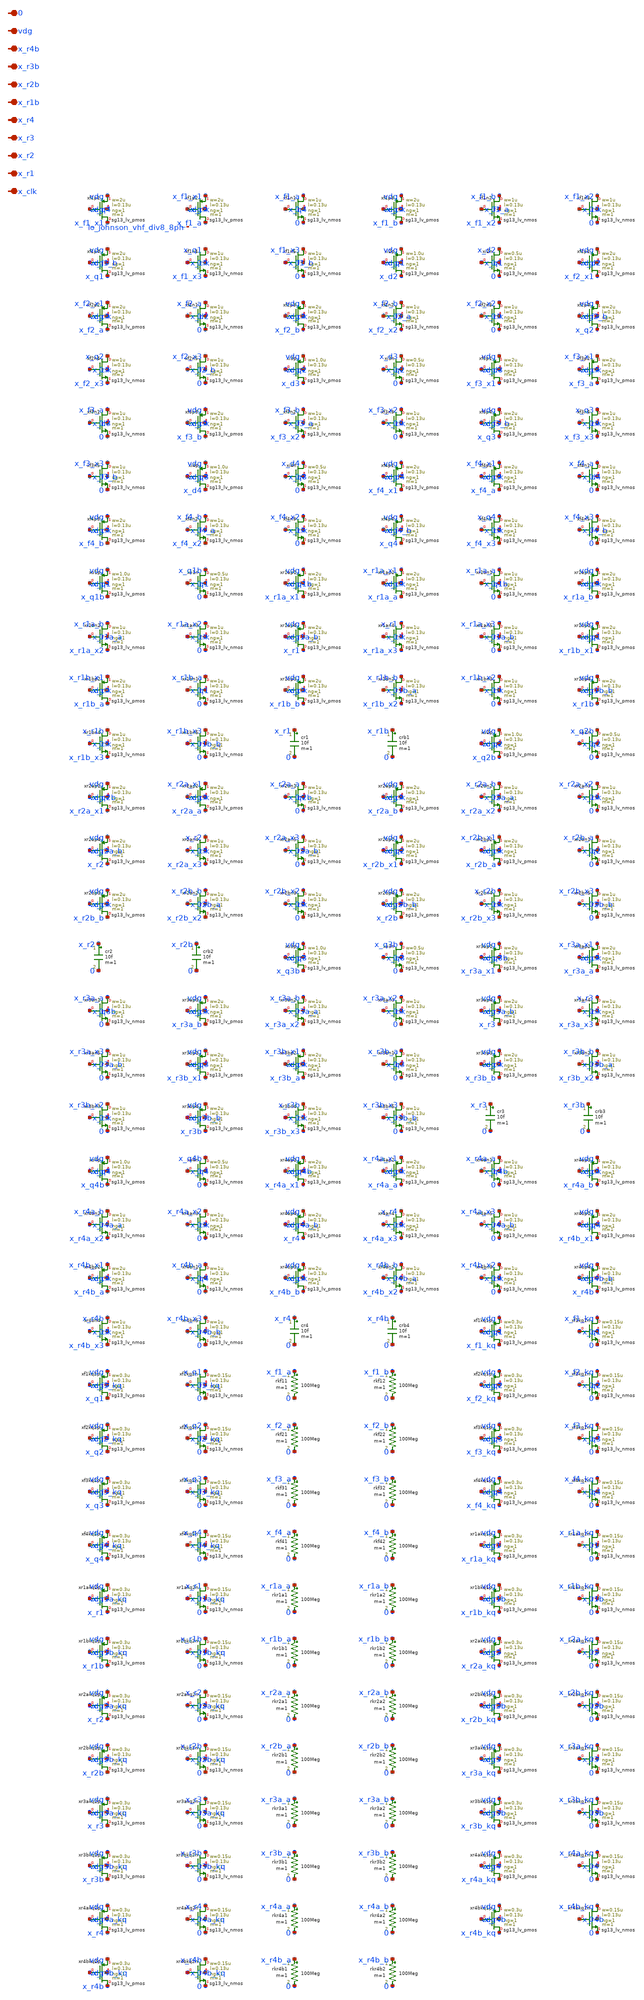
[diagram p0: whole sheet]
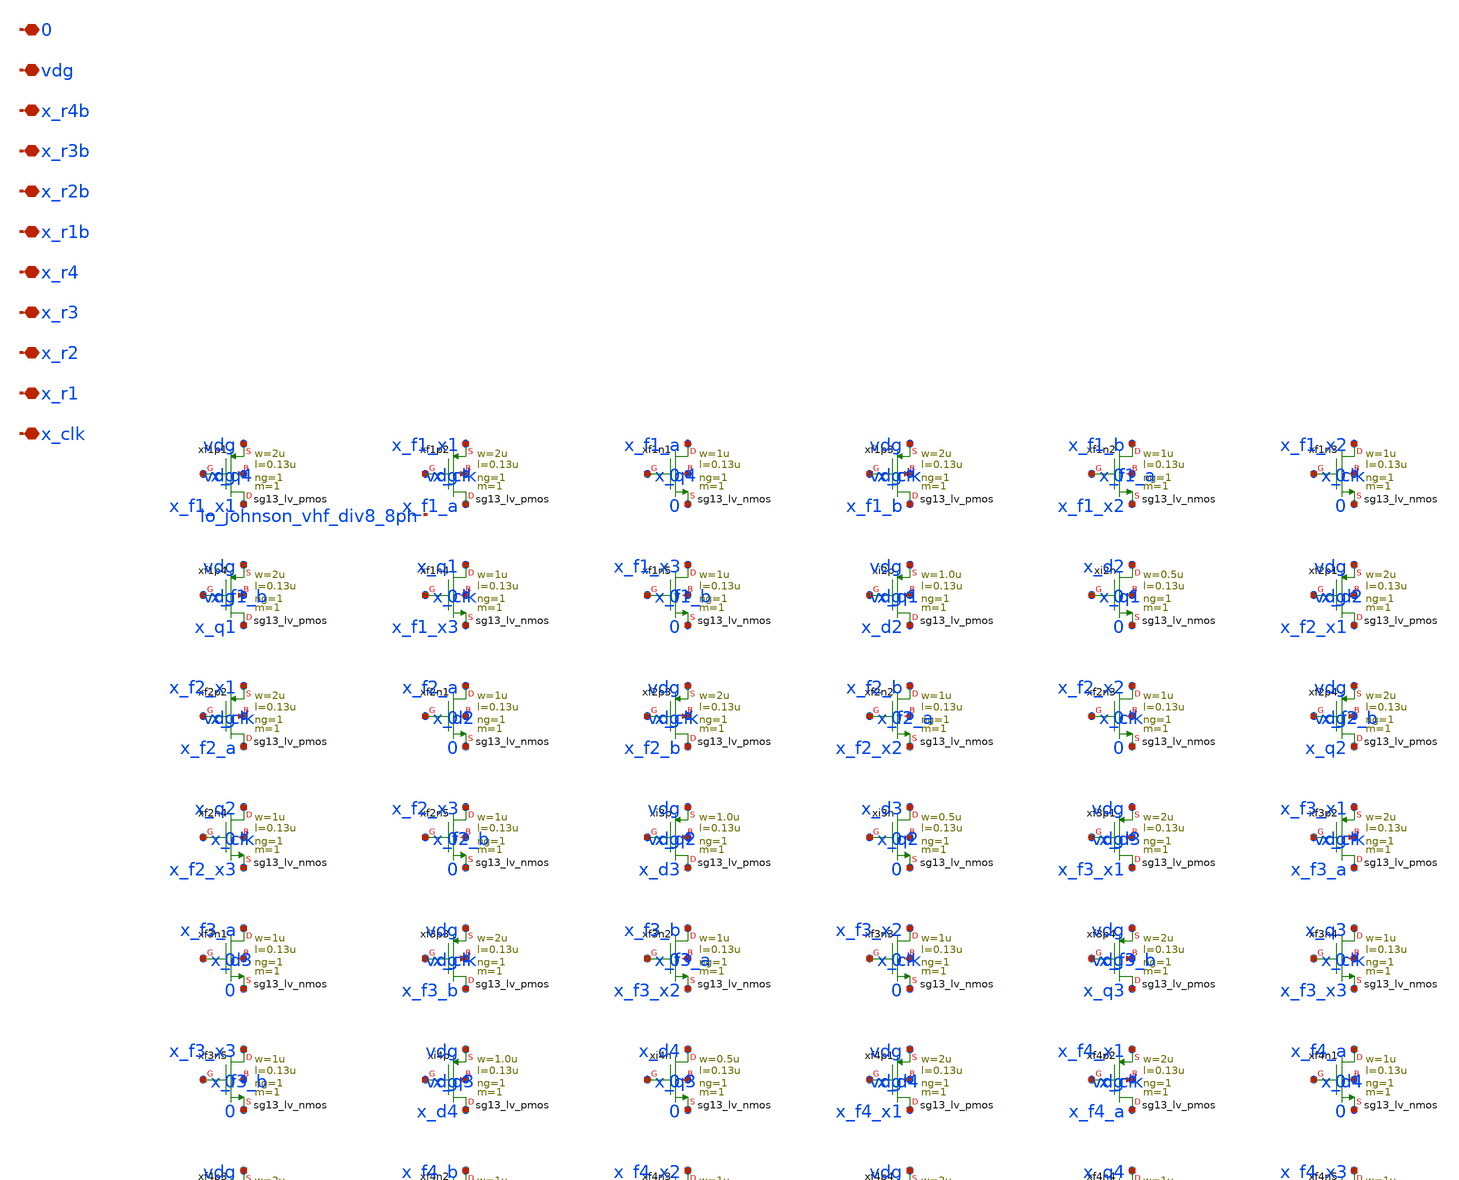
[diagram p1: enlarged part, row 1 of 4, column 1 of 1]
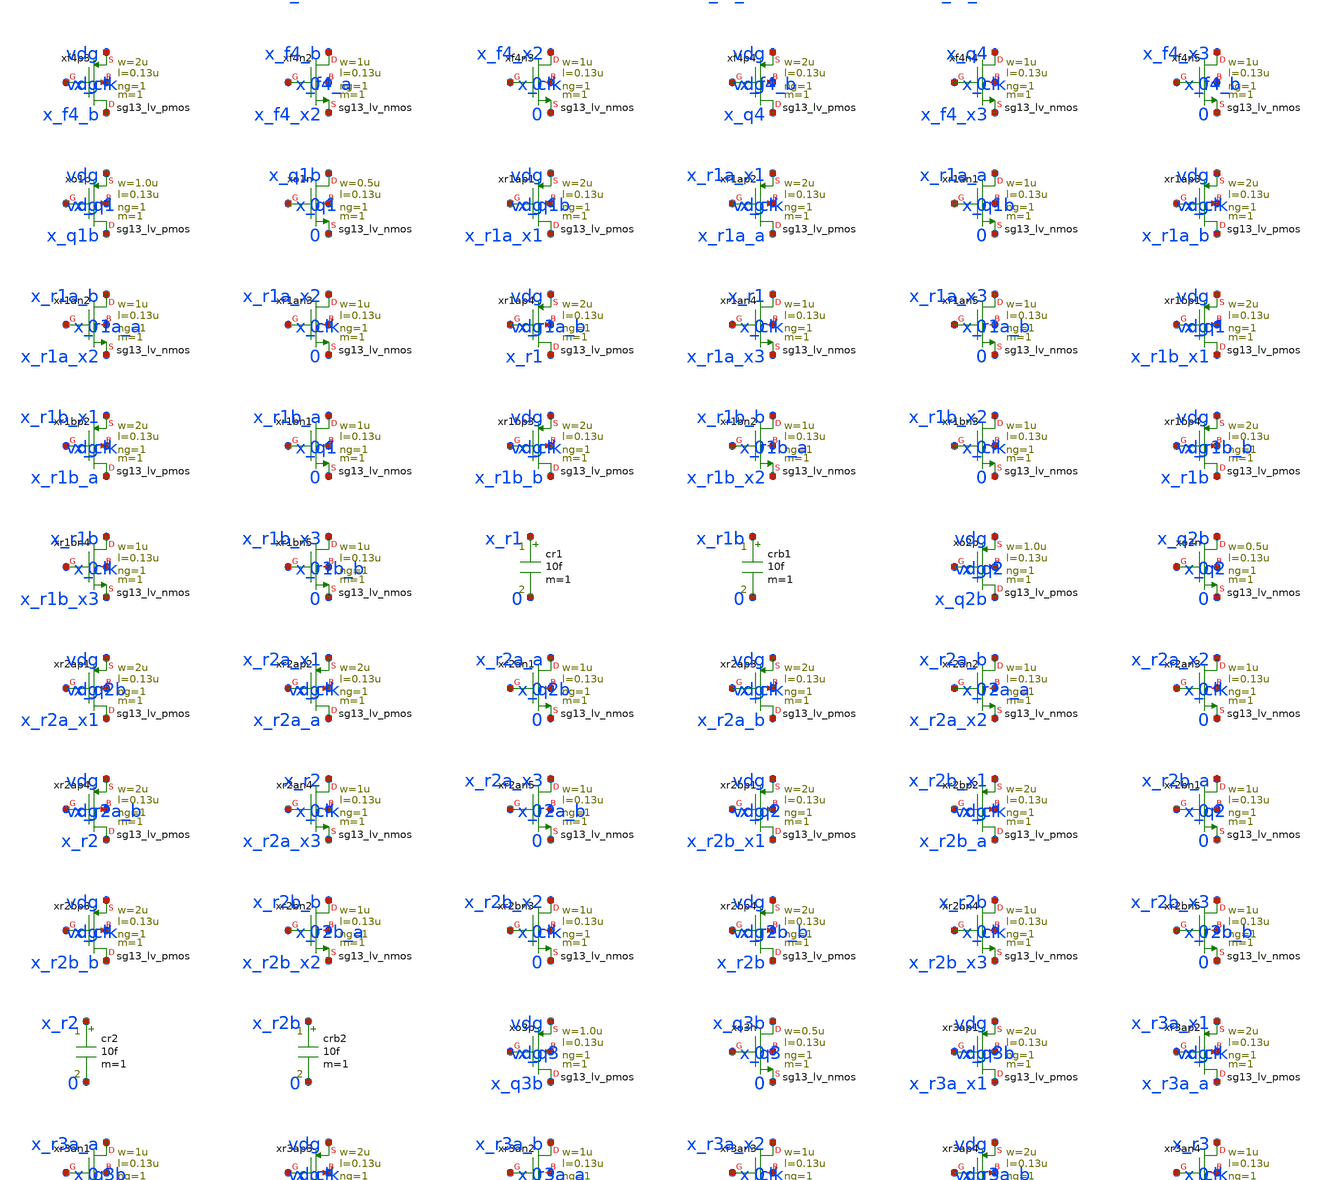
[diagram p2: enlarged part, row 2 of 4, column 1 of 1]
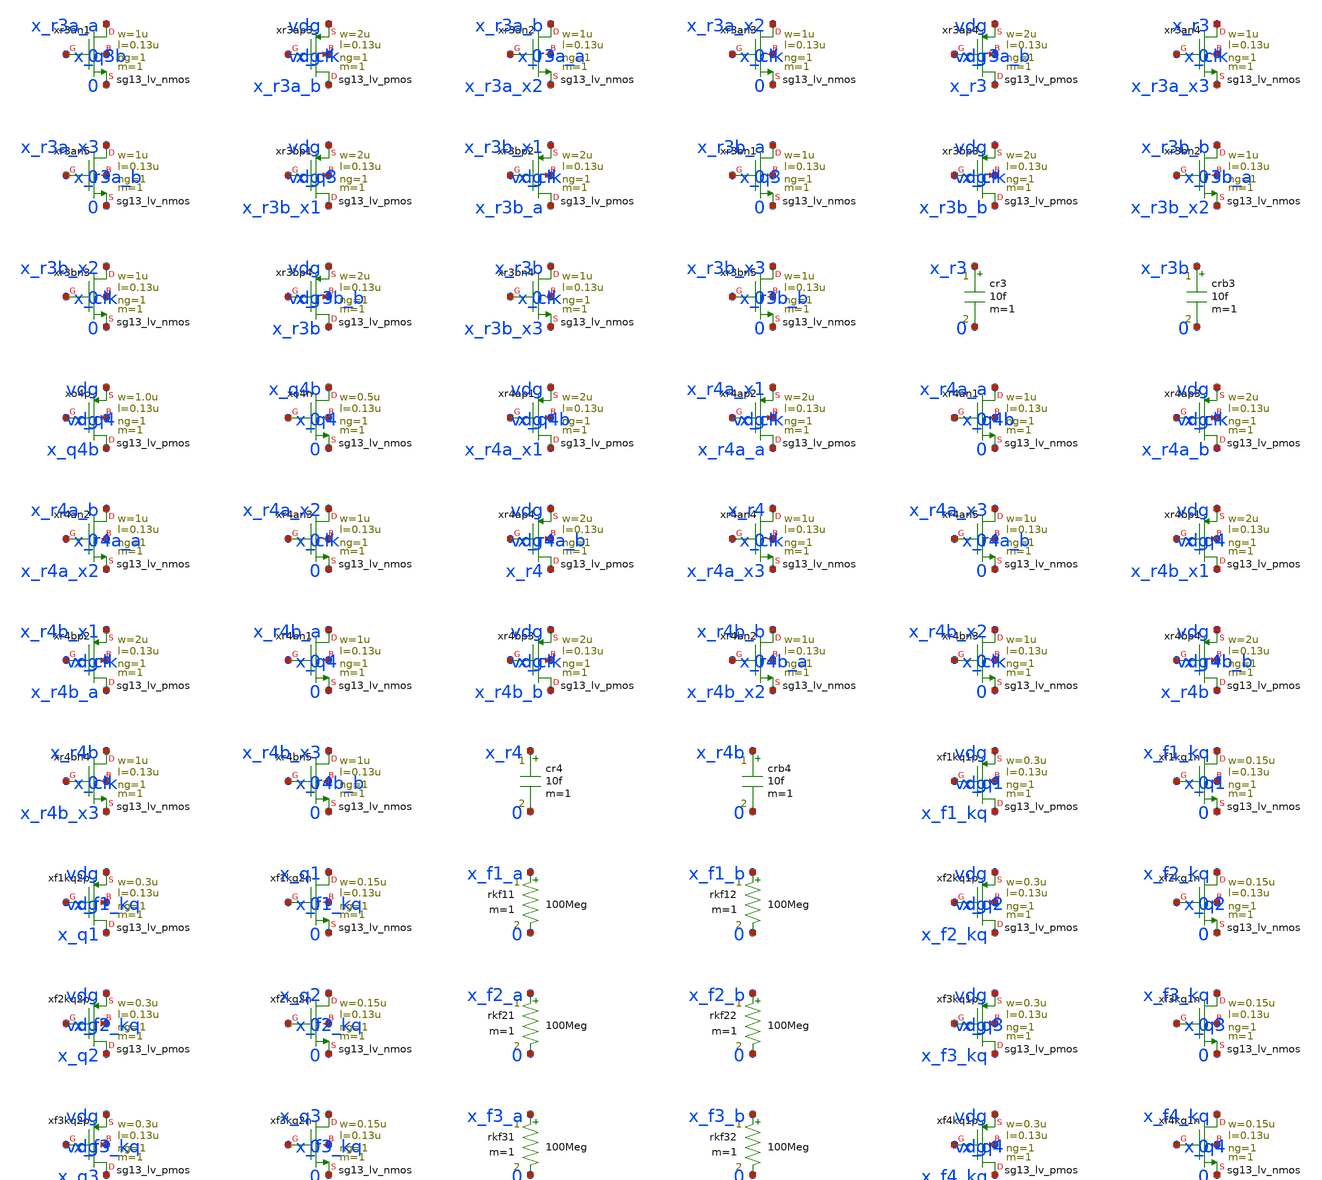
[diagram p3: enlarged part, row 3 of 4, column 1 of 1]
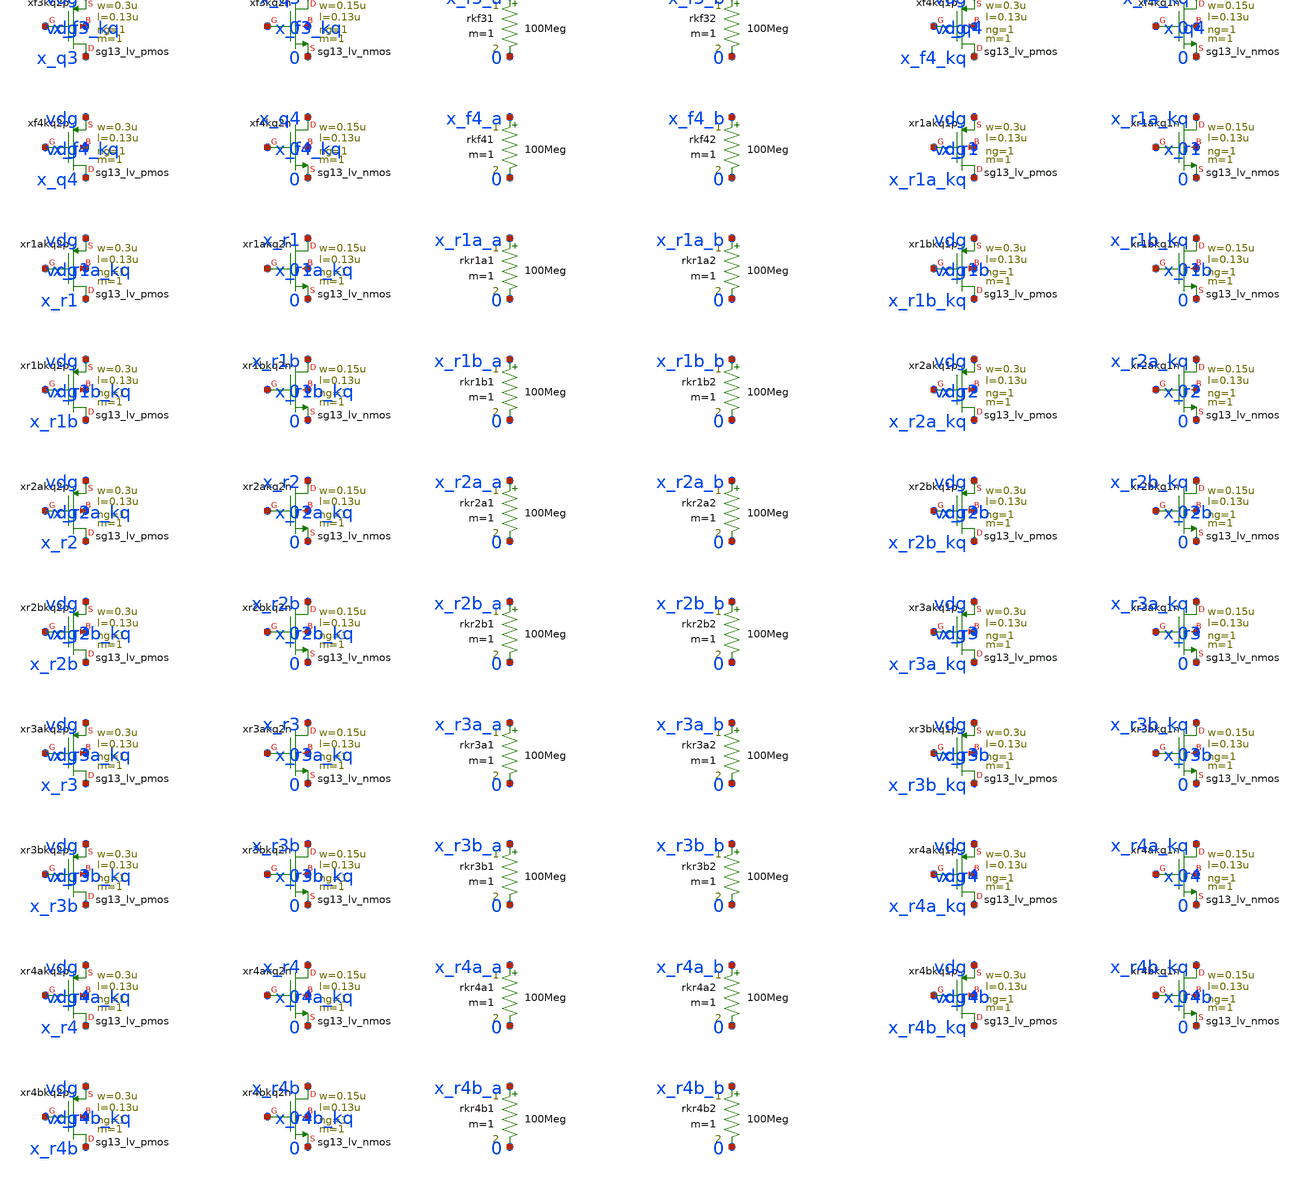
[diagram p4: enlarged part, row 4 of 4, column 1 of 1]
** sch_path: analog/lo/sch/lo_johnson_vhf.sch
**.subckt lo_johnson_vhf x_clk x_r1 x_r2 x_r3 x_r4 x_r1b x_r2b x_r3b x_r4b vdg 0
*.iopin x_clk
*.iopin x_r1
*.iopin x_r2
*.iopin x_r3
*.iopin x_r4
*.iopin x_r1b
*.iopin x_r2b
*.iopin x_r3b
*.iopin x_r4b
*.iopin vdg
*.iopin 0
Xxf1p1 x_f1_x1 x_q4 vdg vdg sg13_lv_pmos w=2u l=0.13u ng=1 m=1 mm_ok=1
Xxf1p2 x_f1_a x_clk x_f1_x1 vdg sg13_lv_pmos w=2u l=0.13u ng=1 m=1 mm_ok=1
Xxf1n1 x_f1_a x_q4 0 0 sg13_lv_nmos w=1u l=0.13u ng=1 m=1 mm_ok=1
Xxf1p3 x_f1_b x_clk vdg vdg sg13_lv_pmos w=2u l=0.13u ng=1 m=1 mm_ok=1
Xxf1n2 x_f1_b x_f1_a x_f1_x2 0 sg13_lv_nmos w=1u l=0.13u ng=1 m=1 mm_ok=1
Xxf1n3 x_f1_x2 x_clk 0 0 sg13_lv_nmos w=1u l=0.13u ng=1 m=1 mm_ok=1
Xxf1p4 x_q1 x_f1_b vdg vdg sg13_lv_pmos w=2u l=0.13u ng=1 m=1 mm_ok=1
Xxf1n4 x_q1 x_clk x_f1_x3 0 sg13_lv_nmos w=1u l=0.13u ng=1 m=1 mm_ok=1
Xxf1n5 x_f1_x3 x_f1_b 0 0 sg13_lv_nmos w=1u l=0.13u ng=1 m=1 mm_ok=1
Xxi2p x_d2 x_q1 vdg vdg sg13_lv_pmos w=1.0u l=0.13u ng=1 m=1 mm_ok=1
Xxi2n x_d2 x_q1 0 0 sg13_lv_nmos w=0.5u l=0.13u ng=1 m=1 mm_ok=1
Xxf2p1 x_f2_x1 x_d2 vdg vdg sg13_lv_pmos w=2u l=0.13u ng=1 m=1 mm_ok=1
Xxf2p2 x_f2_a x_clk x_f2_x1 vdg sg13_lv_pmos w=2u l=0.13u ng=1 m=1 mm_ok=1
Xxf2n1 x_f2_a x_d2 0 0 sg13_lv_nmos w=1u l=0.13u ng=1 m=1 mm_ok=1
Xxf2p3 x_f2_b x_clk vdg vdg sg13_lv_pmos w=2u l=0.13u ng=1 m=1 mm_ok=1
Xxf2n2 x_f2_b x_f2_a x_f2_x2 0 sg13_lv_nmos w=1u l=0.13u ng=1 m=1 mm_ok=1
Xxf2n3 x_f2_x2 x_clk 0 0 sg13_lv_nmos w=1u l=0.13u ng=1 m=1 mm_ok=1
Xxf2p4 x_q2 x_f2_b vdg vdg sg13_lv_pmos w=2u l=0.13u ng=1 m=1 mm_ok=1
Xxf2n4 x_q2 x_clk x_f2_x3 0 sg13_lv_nmos w=1u l=0.13u ng=1 m=1 mm_ok=1
Xxf2n5 x_f2_x3 x_f2_b 0 0 sg13_lv_nmos w=1u l=0.13u ng=1 m=1 mm_ok=1
Xxi3p x_d3 x_q2 vdg vdg sg13_lv_pmos w=1.0u l=0.13u ng=1 m=1 mm_ok=1
Xxi3n x_d3 x_q2 0 0 sg13_lv_nmos w=0.5u l=0.13u ng=1 m=1 mm_ok=1
Xxf3p1 x_f3_x1 x_d3 vdg vdg sg13_lv_pmos w=2u l=0.13u ng=1 m=1 mm_ok=1
Xxf3p2 x_f3_a x_clk x_f3_x1 vdg sg13_lv_pmos w=2u l=0.13u ng=1 m=1 mm_ok=1
Xxf3n1 x_f3_a x_d3 0 0 sg13_lv_nmos w=1u l=0.13u ng=1 m=1 mm_ok=1
Xxf3p3 x_f3_b x_clk vdg vdg sg13_lv_pmos w=2u l=0.13u ng=1 m=1 mm_ok=1
Xxf3n2 x_f3_b x_f3_a x_f3_x2 0 sg13_lv_nmos w=1u l=0.13u ng=1 m=1 mm_ok=1
Xxf3n3 x_f3_x2 x_clk 0 0 sg13_lv_nmos w=1u l=0.13u ng=1 m=1 mm_ok=1
Xxf3p4 x_q3 x_f3_b vdg vdg sg13_lv_pmos w=2u l=0.13u ng=1 m=1 mm_ok=1
Xxf3n4 x_q3 x_clk x_f3_x3 0 sg13_lv_nmos w=1u l=0.13u ng=1 m=1 mm_ok=1
Xxf3n5 x_f3_x3 x_f3_b 0 0 sg13_lv_nmos w=1u l=0.13u ng=1 m=1 mm_ok=1
Xxi4p x_d4 x_q3 vdg vdg sg13_lv_pmos w=1.0u l=0.13u ng=1 m=1 mm_ok=1
Xxi4n x_d4 x_q3 0 0 sg13_lv_nmos w=0.5u l=0.13u ng=1 m=1 mm_ok=1
Xxf4p1 x_f4_x1 x_d4 vdg vdg sg13_lv_pmos w=2u l=0.13u ng=1 m=1 mm_ok=1
Xxf4p2 x_f4_a x_clk x_f4_x1 vdg sg13_lv_pmos w=2u l=0.13u ng=1 m=1 mm_ok=1
Xxf4n1 x_f4_a x_d4 0 0 sg13_lv_nmos w=1u l=0.13u ng=1 m=1 mm_ok=1
Xxf4p3 x_f4_b x_clk vdg vdg sg13_lv_pmos w=2u l=0.13u ng=1 m=1 mm_ok=1
Xxf4n2 x_f4_b x_f4_a x_f4_x2 0 sg13_lv_nmos w=1u l=0.13u ng=1 m=1 mm_ok=1
Xxf4n3 x_f4_x2 x_clk 0 0 sg13_lv_nmos w=1u l=0.13u ng=1 m=1 mm_ok=1
Xxf4p4 x_q4 x_f4_b vdg vdg sg13_lv_pmos w=2u l=0.13u ng=1 m=1 mm_ok=1
Xxf4n4 x_q4 x_clk x_f4_x3 0 sg13_lv_nmos w=1u l=0.13u ng=1 m=1 mm_ok=1
Xxf4n5 x_f4_x3 x_f4_b 0 0 sg13_lv_nmos w=1u l=0.13u ng=1 m=1 mm_ok=1
Xxo1p x_q1b x_q1 vdg vdg sg13_lv_pmos w=1.0u l=0.13u ng=1 m=1 mm_ok=1
Xxo1n x_q1b x_q1 0 0 sg13_lv_nmos w=0.5u l=0.13u ng=1 m=1 mm_ok=1
Xxr1ap1 x_r1a_x1 x_q1b vdg vdg sg13_lv_pmos w=2u l=0.13u ng=1 m=1 mm_ok=1
Xxr1ap2 x_r1a_a x_clk x_r1a_x1 vdg sg13_lv_pmos w=2u l=0.13u ng=1 m=1 mm_ok=1
Xxr1an1 x_r1a_a x_q1b 0 0 sg13_lv_nmos w=1u l=0.13u ng=1 m=1 mm_ok=1
Xxr1ap3 x_r1a_b x_clk vdg vdg sg13_lv_pmos w=2u l=0.13u ng=1 m=1 mm_ok=1
Xxr1an2 x_r1a_b x_r1a_a x_r1a_x2 0 sg13_lv_nmos w=1u l=0.13u ng=1 m=1 mm_ok=1
Xxr1an3 x_r1a_x2 x_clk 0 0 sg13_lv_nmos w=1u l=0.13u ng=1 m=1 mm_ok=1
Xxr1ap4 x_r1 x_r1a_b vdg vdg sg13_lv_pmos w=2u l=0.13u ng=1 m=1 mm_ok=1
Xxr1an4 x_r1 x_clk x_r1a_x3 0 sg13_lv_nmos w=1u l=0.13u ng=1 m=1 mm_ok=1
Xxr1an5 x_r1a_x3 x_r1a_b 0 0 sg13_lv_nmos w=1u l=0.13u ng=1 m=1 mm_ok=1
Xxr1bp1 x_r1b_x1 x_q1 vdg vdg sg13_lv_pmos w=2u l=0.13u ng=1 m=1 mm_ok=1
Xxr1bp2 x_r1b_a x_clk x_r1b_x1 vdg sg13_lv_pmos w=2u l=0.13u ng=1 m=1 mm_ok=1
Xxr1bn1 x_r1b_a x_q1 0 0 sg13_lv_nmos w=1u l=0.13u ng=1 m=1 mm_ok=1
Xxr1bp3 x_r1b_b x_clk vdg vdg sg13_lv_pmos w=2u l=0.13u ng=1 m=1 mm_ok=1
Xxr1bn2 x_r1b_b x_r1b_a x_r1b_x2 0 sg13_lv_nmos w=1u l=0.13u ng=1 m=1 mm_ok=1
Xxr1bn3 x_r1b_x2 x_clk 0 0 sg13_lv_nmos w=1u l=0.13u ng=1 m=1 mm_ok=1
Xxr1bp4 x_r1b x_r1b_b vdg vdg sg13_lv_pmos w=2u l=0.13u ng=1 m=1 mm_ok=1
Xxr1bn4 x_r1b x_clk x_r1b_x3 0 sg13_lv_nmos w=1u l=0.13u ng=1 m=1 mm_ok=1
Xxr1bn5 x_r1b_x3 x_r1b_b 0 0 sg13_lv_nmos w=1u l=0.13u ng=1 m=1 mm_ok=1
cr1 x_r1 0 10f m=1
crb1 x_r1b 0 10f m=1
Xxo2p x_q2b x_q2 vdg vdg sg13_lv_pmos w=1.0u l=0.13u ng=1 m=1 mm_ok=1
Xxo2n x_q2b x_q2 0 0 sg13_lv_nmos w=0.5u l=0.13u ng=1 m=1 mm_ok=1
Xxr2ap1 x_r2a_x1 x_q2b vdg vdg sg13_lv_pmos w=2u l=0.13u ng=1 m=1 mm_ok=1
Xxr2ap2 x_r2a_a x_clk x_r2a_x1 vdg sg13_lv_pmos w=2u l=0.13u ng=1 m=1 mm_ok=1
Xxr2an1 x_r2a_a x_q2b 0 0 sg13_lv_nmos w=1u l=0.13u ng=1 m=1 mm_ok=1
Xxr2ap3 x_r2a_b x_clk vdg vdg sg13_lv_pmos w=2u l=0.13u ng=1 m=1 mm_ok=1
Xxr2an2 x_r2a_b x_r2a_a x_r2a_x2 0 sg13_lv_nmos w=1u l=0.13u ng=1 m=1 mm_ok=1
Xxr2an3 x_r2a_x2 x_clk 0 0 sg13_lv_nmos w=1u l=0.13u ng=1 m=1 mm_ok=1
Xxr2ap4 x_r2 x_r2a_b vdg vdg sg13_lv_pmos w=2u l=0.13u ng=1 m=1 mm_ok=1
Xxr2an4 x_r2 x_clk x_r2a_x3 0 sg13_lv_nmos w=1u l=0.13u ng=1 m=1 mm_ok=1
Xxr2an5 x_r2a_x3 x_r2a_b 0 0 sg13_lv_nmos w=1u l=0.13u ng=1 m=1 mm_ok=1
Xxr2bp1 x_r2b_x1 x_q2 vdg vdg sg13_lv_pmos w=2u l=0.13u ng=1 m=1 mm_ok=1
Xxr2bp2 x_r2b_a x_clk x_r2b_x1 vdg sg13_lv_pmos w=2u l=0.13u ng=1 m=1 mm_ok=1
Xxr2bn1 x_r2b_a x_q2 0 0 sg13_lv_nmos w=1u l=0.13u ng=1 m=1 mm_ok=1
Xxr2bp3 x_r2b_b x_clk vdg vdg sg13_lv_pmos w=2u l=0.13u ng=1 m=1 mm_ok=1
Xxr2bn2 x_r2b_b x_r2b_a x_r2b_x2 0 sg13_lv_nmos w=1u l=0.13u ng=1 m=1 mm_ok=1
Xxr2bn3 x_r2b_x2 x_clk 0 0 sg13_lv_nmos w=1u l=0.13u ng=1 m=1 mm_ok=1
Xxr2bp4 x_r2b x_r2b_b vdg vdg sg13_lv_pmos w=2u l=0.13u ng=1 m=1 mm_ok=1
Xxr2bn4 x_r2b x_clk x_r2b_x3 0 sg13_lv_nmos w=1u l=0.13u ng=1 m=1 mm_ok=1
Xxr2bn5 x_r2b_x3 x_r2b_b 0 0 sg13_lv_nmos w=1u l=0.13u ng=1 m=1 mm_ok=1
cr2 x_r2 0 10f m=1
crb2 x_r2b 0 10f m=1
Xxo3p x_q3b x_q3 vdg vdg sg13_lv_pmos w=1.0u l=0.13u ng=1 m=1 mm_ok=1
Xxo3n x_q3b x_q3 0 0 sg13_lv_nmos w=0.5u l=0.13u ng=1 m=1 mm_ok=1
Xxr3ap1 x_r3a_x1 x_q3b vdg vdg sg13_lv_pmos w=2u l=0.13u ng=1 m=1 mm_ok=1
Xxr3ap2 x_r3a_a x_clk x_r3a_x1 vdg sg13_lv_pmos w=2u l=0.13u ng=1 m=1 mm_ok=1
Xxr3an1 x_r3a_a x_q3b 0 0 sg13_lv_nmos w=1u l=0.13u ng=1 m=1 mm_ok=1
Xxr3ap3 x_r3a_b x_clk vdg vdg sg13_lv_pmos w=2u l=0.13u ng=1 m=1 mm_ok=1
Xxr3an2 x_r3a_b x_r3a_a x_r3a_x2 0 sg13_lv_nmos w=1u l=0.13u ng=1 m=1 mm_ok=1
Xxr3an3 x_r3a_x2 x_clk 0 0 sg13_lv_nmos w=1u l=0.13u ng=1 m=1 mm_ok=1
Xxr3ap4 x_r3 x_r3a_b vdg vdg sg13_lv_pmos w=2u l=0.13u ng=1 m=1 mm_ok=1
Xxr3an4 x_r3 x_clk x_r3a_x3 0 sg13_lv_nmos w=1u l=0.13u ng=1 m=1 mm_ok=1
Xxr3an5 x_r3a_x3 x_r3a_b 0 0 sg13_lv_nmos w=1u l=0.13u ng=1 m=1 mm_ok=1
Xxr3bp1 x_r3b_x1 x_q3 vdg vdg sg13_lv_pmos w=2u l=0.13u ng=1 m=1 mm_ok=1
Xxr3bp2 x_r3b_a x_clk x_r3b_x1 vdg sg13_lv_pmos w=2u l=0.13u ng=1 m=1 mm_ok=1
Xxr3bn1 x_r3b_a x_q3 0 0 sg13_lv_nmos w=1u l=0.13u ng=1 m=1 mm_ok=1
Xxr3bp3 x_r3b_b x_clk vdg vdg sg13_lv_pmos w=2u l=0.13u ng=1 m=1 mm_ok=1
Xxr3bn2 x_r3b_b x_r3b_a x_r3b_x2 0 sg13_lv_nmos w=1u l=0.13u ng=1 m=1 mm_ok=1
Xxr3bn3 x_r3b_x2 x_clk 0 0 sg13_lv_nmos w=1u l=0.13u ng=1 m=1 mm_ok=1
Xxr3bp4 x_r3b x_r3b_b vdg vdg sg13_lv_pmos w=2u l=0.13u ng=1 m=1 mm_ok=1
Xxr3bn4 x_r3b x_clk x_r3b_x3 0 sg13_lv_nmos w=1u l=0.13u ng=1 m=1 mm_ok=1
Xxr3bn5 x_r3b_x3 x_r3b_b 0 0 sg13_lv_nmos w=1u l=0.13u ng=1 m=1 mm_ok=1
cr3 x_r3 0 10f m=1
crb3 x_r3b 0 10f m=1
Xxo4p x_q4b x_q4 vdg vdg sg13_lv_pmos w=1.0u l=0.13u ng=1 m=1 mm_ok=1
Xxo4n x_q4b x_q4 0 0 sg13_lv_nmos w=0.5u l=0.13u ng=1 m=1 mm_ok=1
Xxr4ap1 x_r4a_x1 x_q4b vdg vdg sg13_lv_pmos w=2u l=0.13u ng=1 m=1 mm_ok=1
Xxr4ap2 x_r4a_a x_clk x_r4a_x1 vdg sg13_lv_pmos w=2u l=0.13u ng=1 m=1 mm_ok=1
Xxr4an1 x_r4a_a x_q4b 0 0 sg13_lv_nmos w=1u l=0.13u ng=1 m=1 mm_ok=1
Xxr4ap3 x_r4a_b x_clk vdg vdg sg13_lv_pmos w=2u l=0.13u ng=1 m=1 mm_ok=1
Xxr4an2 x_r4a_b x_r4a_a x_r4a_x2 0 sg13_lv_nmos w=1u l=0.13u ng=1 m=1 mm_ok=1
Xxr4an3 x_r4a_x2 x_clk 0 0 sg13_lv_nmos w=1u l=0.13u ng=1 m=1 mm_ok=1
Xxr4ap4 x_r4 x_r4a_b vdg vdg sg13_lv_pmos w=2u l=0.13u ng=1 m=1 mm_ok=1
Xxr4an4 x_r4 x_clk x_r4a_x3 0 sg13_lv_nmos w=1u l=0.13u ng=1 m=1 mm_ok=1
Xxr4an5 x_r4a_x3 x_r4a_b 0 0 sg13_lv_nmos w=1u l=0.13u ng=1 m=1 mm_ok=1
Xxr4bp1 x_r4b_x1 x_q4 vdg vdg sg13_lv_pmos w=2u l=0.13u ng=1 m=1 mm_ok=1
Xxr4bp2 x_r4b_a x_clk x_r4b_x1 vdg sg13_lv_pmos w=2u l=0.13u ng=1 m=1 mm_ok=1
Xxr4bn1 x_r4b_a x_q4 0 0 sg13_lv_nmos w=1u l=0.13u ng=1 m=1 mm_ok=1
Xxr4bp3 x_r4b_b x_clk vdg vdg sg13_lv_pmos w=2u l=0.13u ng=1 m=1 mm_ok=1
Xxr4bn2 x_r4b_b x_r4b_a x_r4b_x2 0 sg13_lv_nmos w=1u l=0.13u ng=1 m=1 mm_ok=1
Xxr4bn3 x_r4b_x2 x_clk 0 0 sg13_lv_nmos w=1u l=0.13u ng=1 m=1 mm_ok=1
Xxr4bp4 x_r4b x_r4b_b vdg vdg sg13_lv_pmos w=2u l=0.13u ng=1 m=1 mm_ok=1
Xxr4bn4 x_r4b x_clk x_r4b_x3 0 sg13_lv_nmos w=1u l=0.13u ng=1 m=1 mm_ok=1
Xxr4bn5 x_r4b_x3 x_r4b_b 0 0 sg13_lv_nmos w=1u l=0.13u ng=1 m=1 mm_ok=1
cr4 x_r4 0 10f m=1
crb4 x_r4b 0 10f m=1
Xxf1kq1p x_f1_kq x_q1 vdg vdg sg13_lv_pmos w=0.3u l=0.13u ng=1 m=1 mm_ok=1
Xxf1kq1n x_f1_kq x_q1 0 0 sg13_lv_nmos w=0.15u l=0.13u ng=1 m=1 mm_ok=1
Xxf1kq2p x_q1 x_f1_kq vdg vdg sg13_lv_pmos w=0.3u l=0.13u ng=1 m=1 mm_ok=1
Xxf1kq2n x_q1 x_f1_kq 0 0 sg13_lv_nmos w=0.15u l=0.13u ng=1 m=1 mm_ok=1
rkf11 x_f1_a 0 100Meg m=1
rkf12 x_f1_b 0 100Meg m=1
Xxf2kq1p x_f2_kq x_q2 vdg vdg sg13_lv_pmos w=0.3u l=0.13u ng=1 m=1 mm_ok=1
Xxf2kq1n x_f2_kq x_q2 0 0 sg13_lv_nmos w=0.15u l=0.13u ng=1 m=1 mm_ok=1
Xxf2kq2p x_q2 x_f2_kq vdg vdg sg13_lv_pmos w=0.3u l=0.13u ng=1 m=1 mm_ok=1
Xxf2kq2n x_q2 x_f2_kq 0 0 sg13_lv_nmos w=0.15u l=0.13u ng=1 m=1 mm_ok=1
rkf21 x_f2_a 0 100Meg m=1
rkf22 x_f2_b 0 100Meg m=1
Xxf3kq1p x_f3_kq x_q3 vdg vdg sg13_lv_pmos w=0.3u l=0.13u ng=1 m=1 mm_ok=1
Xxf3kq1n x_f3_kq x_q3 0 0 sg13_lv_nmos w=0.15u l=0.13u ng=1 m=1 mm_ok=1
Xxf3kq2p x_q3 x_f3_kq vdg vdg sg13_lv_pmos w=0.3u l=0.13u ng=1 m=1 mm_ok=1
Xxf3kq2n x_q3 x_f3_kq 0 0 sg13_lv_nmos w=0.15u l=0.13u ng=1 m=1 mm_ok=1
rkf31 x_f3_a 0 100Meg m=1
rkf32 x_f3_b 0 100Meg m=1
Xxf4kq1p x_f4_kq x_q4 vdg vdg sg13_lv_pmos w=0.3u l=0.13u ng=1 m=1 mm_ok=1
Xxf4kq1n x_f4_kq x_q4 0 0 sg13_lv_nmos w=0.15u l=0.13u ng=1 m=1 mm_ok=1
Xxf4kq2p x_q4 x_f4_kq vdg vdg sg13_lv_pmos w=0.3u l=0.13u ng=1 m=1 mm_ok=1
Xxf4kq2n x_q4 x_f4_kq 0 0 sg13_lv_nmos w=0.15u l=0.13u ng=1 m=1 mm_ok=1
rkf41 x_f4_a 0 100Meg m=1
rkf42 x_f4_b 0 100Meg m=1
Xxr1akq1p x_r1a_kq x_r1 vdg vdg sg13_lv_pmos w=0.3u l=0.13u ng=1 m=1 mm_ok=1
Xxr1akq1n x_r1a_kq x_r1 0 0 sg13_lv_nmos w=0.15u l=0.13u ng=1 m=1 mm_ok=1
Xxr1akq2p x_r1 x_r1a_kq vdg vdg sg13_lv_pmos w=0.3u l=0.13u ng=1 m=1 mm_ok=1
Xxr1akq2n x_r1 x_r1a_kq 0 0 sg13_lv_nmos w=0.15u l=0.13u ng=1 m=1 mm_ok=1
rkr1a1 x_r1a_a 0 100Meg m=1
rkr1a2 x_r1a_b 0 100Meg m=1
Xxr1bkq1p x_r1b_kq x_r1b vdg vdg sg13_lv_pmos w=0.3u l=0.13u ng=1 m=1 mm_ok=1
Xxr1bkq1n x_r1b_kq x_r1b 0 0 sg13_lv_nmos w=0.15u l=0.13u ng=1 m=1 mm_ok=1
Xxr1bkq2p x_r1b x_r1b_kq vdg vdg sg13_lv_pmos w=0.3u l=0.13u ng=1 m=1 mm_ok=1
Xxr1bkq2n x_r1b x_r1b_kq 0 0 sg13_lv_nmos w=0.15u l=0.13u ng=1 m=1 mm_ok=1
rkr1b1 x_r1b_a 0 100Meg m=1
rkr1b2 x_r1b_b 0 100Meg m=1
Xxr2akq1p x_r2a_kq x_r2 vdg vdg sg13_lv_pmos w=0.3u l=0.13u ng=1 m=1 mm_ok=1
Xxr2akq1n x_r2a_kq x_r2 0 0 sg13_lv_nmos w=0.15u l=0.13u ng=1 m=1 mm_ok=1
Xxr2akq2p x_r2 x_r2a_kq vdg vdg sg13_lv_pmos w=0.3u l=0.13u ng=1 m=1 mm_ok=1
Xxr2akq2n x_r2 x_r2a_kq 0 0 sg13_lv_nmos w=0.15u l=0.13u ng=1 m=1 mm_ok=1
rkr2a1 x_r2a_a 0 100Meg m=1
rkr2a2 x_r2a_b 0 100Meg m=1
Xxr2bkq1p x_r2b_kq x_r2b vdg vdg sg13_lv_pmos w=0.3u l=0.13u ng=1 m=1 mm_ok=1
Xxr2bkq1n x_r2b_kq x_r2b 0 0 sg13_lv_nmos w=0.15u l=0.13u ng=1 m=1 mm_ok=1
Xxr2bkq2p x_r2b x_r2b_kq vdg vdg sg13_lv_pmos w=0.3u l=0.13u ng=1 m=1 mm_ok=1
Xxr2bkq2n x_r2b x_r2b_kq 0 0 sg13_lv_nmos w=0.15u l=0.13u ng=1 m=1 mm_ok=1
rkr2b1 x_r2b_a 0 100Meg m=1
rkr2b2 x_r2b_b 0 100Meg m=1
Xxr3akq1p x_r3a_kq x_r3 vdg vdg sg13_lv_pmos w=0.3u l=0.13u ng=1 m=1 mm_ok=1
Xxr3akq1n x_r3a_kq x_r3 0 0 sg13_lv_nmos w=0.15u l=0.13u ng=1 m=1 mm_ok=1
Xxr3akq2p x_r3 x_r3a_kq vdg vdg sg13_lv_pmos w=0.3u l=0.13u ng=1 m=1 mm_ok=1
Xxr3akq2n x_r3 x_r3a_kq 0 0 sg13_lv_nmos w=0.15u l=0.13u ng=1 m=1 mm_ok=1
rkr3a1 x_r3a_a 0 100Meg m=1
rkr3a2 x_r3a_b 0 100Meg m=1
Xxr3bkq1p x_r3b_kq x_r3b vdg vdg sg13_lv_pmos w=0.3u l=0.13u ng=1 m=1 mm_ok=1
Xxr3bkq1n x_r3b_kq x_r3b 0 0 sg13_lv_nmos w=0.15u l=0.13u ng=1 m=1 mm_ok=1
Xxr3bkq2p x_r3b x_r3b_kq vdg vdg sg13_lv_pmos w=0.3u l=0.13u ng=1 m=1 mm_ok=1
Xxr3bkq2n x_r3b x_r3b_kq 0 0 sg13_lv_nmos w=0.15u l=0.13u ng=1 m=1 mm_ok=1
rkr3b1 x_r3b_a 0 100Meg m=1
rkr3b2 x_r3b_b 0 100Meg m=1
Xxr4akq1p x_r4a_kq x_r4 vdg vdg sg13_lv_pmos w=0.3u l=0.13u ng=1 m=1 mm_ok=1
Xxr4akq1n x_r4a_kq x_r4 0 0 sg13_lv_nmos w=0.15u l=0.13u ng=1 m=1 mm_ok=1
Xxr4akq2p x_r4 x_r4a_kq vdg vdg sg13_lv_pmos w=0.3u l=0.13u ng=1 m=1 mm_ok=1
Xxr4akq2n x_r4 x_r4a_kq 0 0 sg13_lv_nmos w=0.15u l=0.13u ng=1 m=1 mm_ok=1
rkr4a1 x_r4a_a 0 100Meg m=1
rkr4a2 x_r4a_b 0 100Meg m=1
Xxr4bkq1p x_r4b_kq x_r4b vdg vdg sg13_lv_pmos w=0.3u l=0.13u ng=1 m=1 mm_ok=1
Xxr4bkq1n x_r4b_kq x_r4b 0 0 sg13_lv_nmos w=0.15u l=0.13u ng=1 m=1 mm_ok=1
Xxr4bkq2p x_r4b x_r4b_kq vdg vdg sg13_lv_pmos w=0.3u l=0.13u ng=1 m=1 mm_ok=1
Xxr4bkq2n x_r4b x_r4b_kq 0 0 sg13_lv_nmos w=0.15u l=0.13u ng=1 m=1 mm_ok=1
rkr4b1 x_r4b_a 0 100Meg m=1
rkr4b2 x_r4b_b 0 100Meg m=1
**.ends
.end
